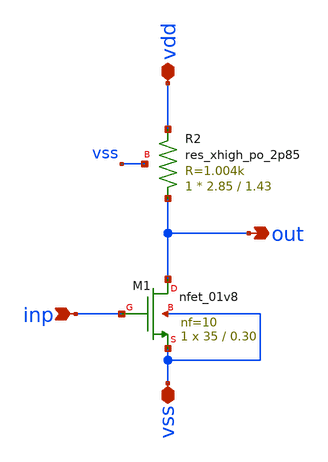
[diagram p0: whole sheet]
** sch_path: xschem/cs.sch
**.subckt cs inp out vdd vss
*.ipin inp
*.opin out
*.iopin vdd
*.iopin vss
XM1 out inp vss vss sky130_fd_pr__nfet_01v8 L=0.30 W=35 nf=10 ad='int((nf+1)/2) * W/nf * 0.29' as='int((nf+2)/2) * W/nf * 0.29'
+ pd='2*int((nf+1)/2) * (W/nf + 0.29)' ps='2*int((nf+2)/2) * (W/nf + 0.29)' nrd='0.29 / W' nrs='0.29 / W'
+ sa=0 sb=0 sd=0 mult=1 m=1
XR2 out vdd vss sky130_fd_pr__res_xhigh_po_2p85 L=1.43 mult=1 m=1
**.ends
.end
